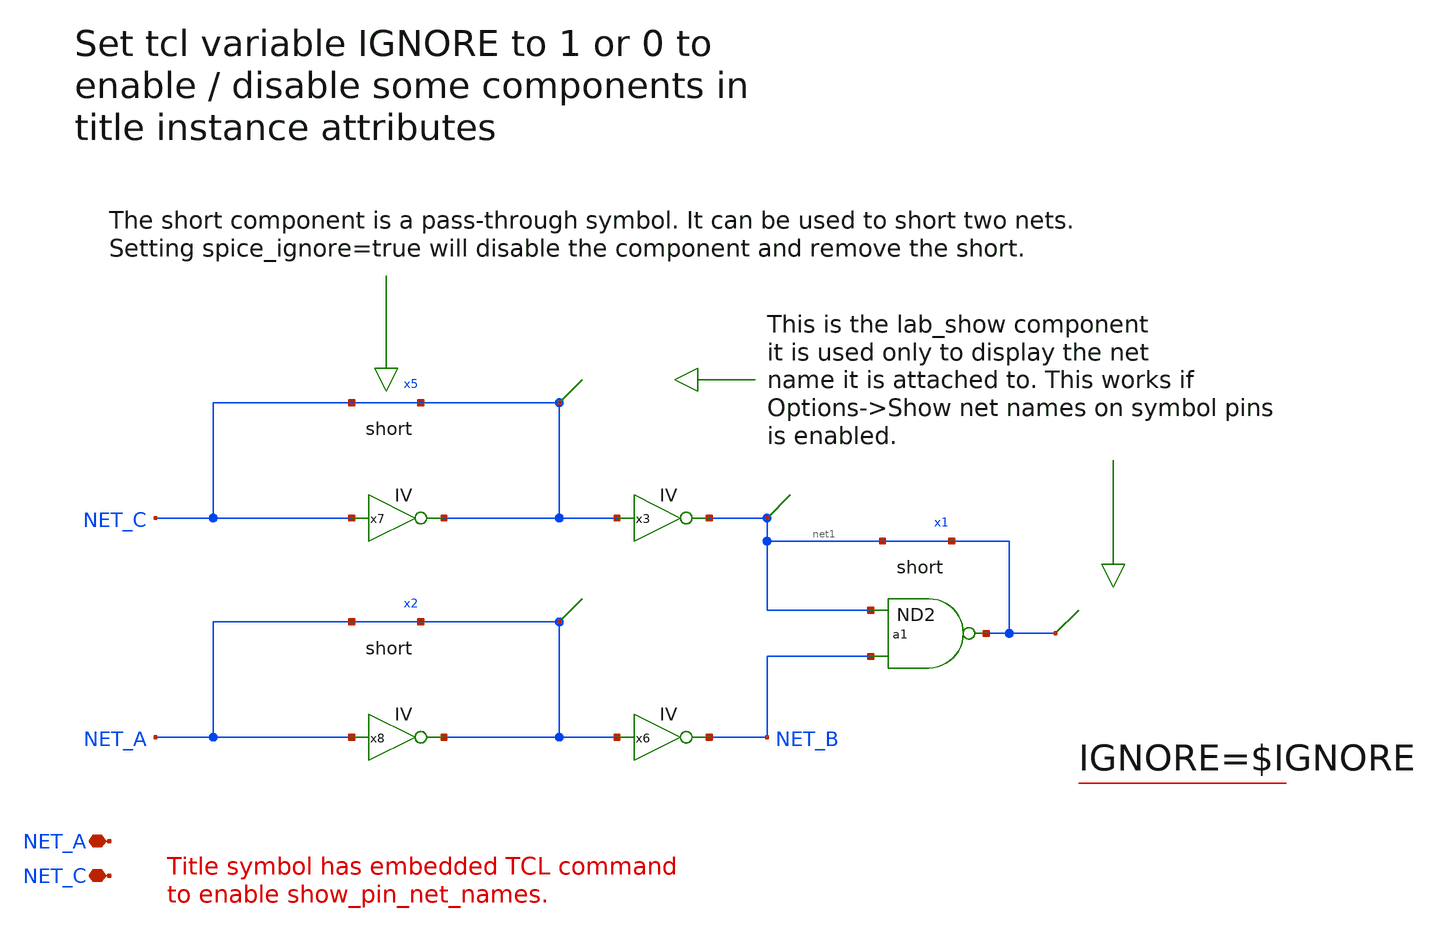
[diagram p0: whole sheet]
** sch_path: xschem_library/examples/test_short_option.sch
**.subckt test_short_option NET_A NET_C
*.iopin NET_A
*.iopin NET_C
* short x2 : NET_A <--> NET_A
* short x5 : NET_C <--> NET_C
x3 [ NET_C ] net1 inv
x6 [ NET_A ] NET_B inv
x7 [ NET_C ] NET_C inv
x8 [ NET_A ] NET_A inv
a1 [ net1 NET_B ] net1 nand
* short x1 : #net1 <--> #net1
**.ends
.end
